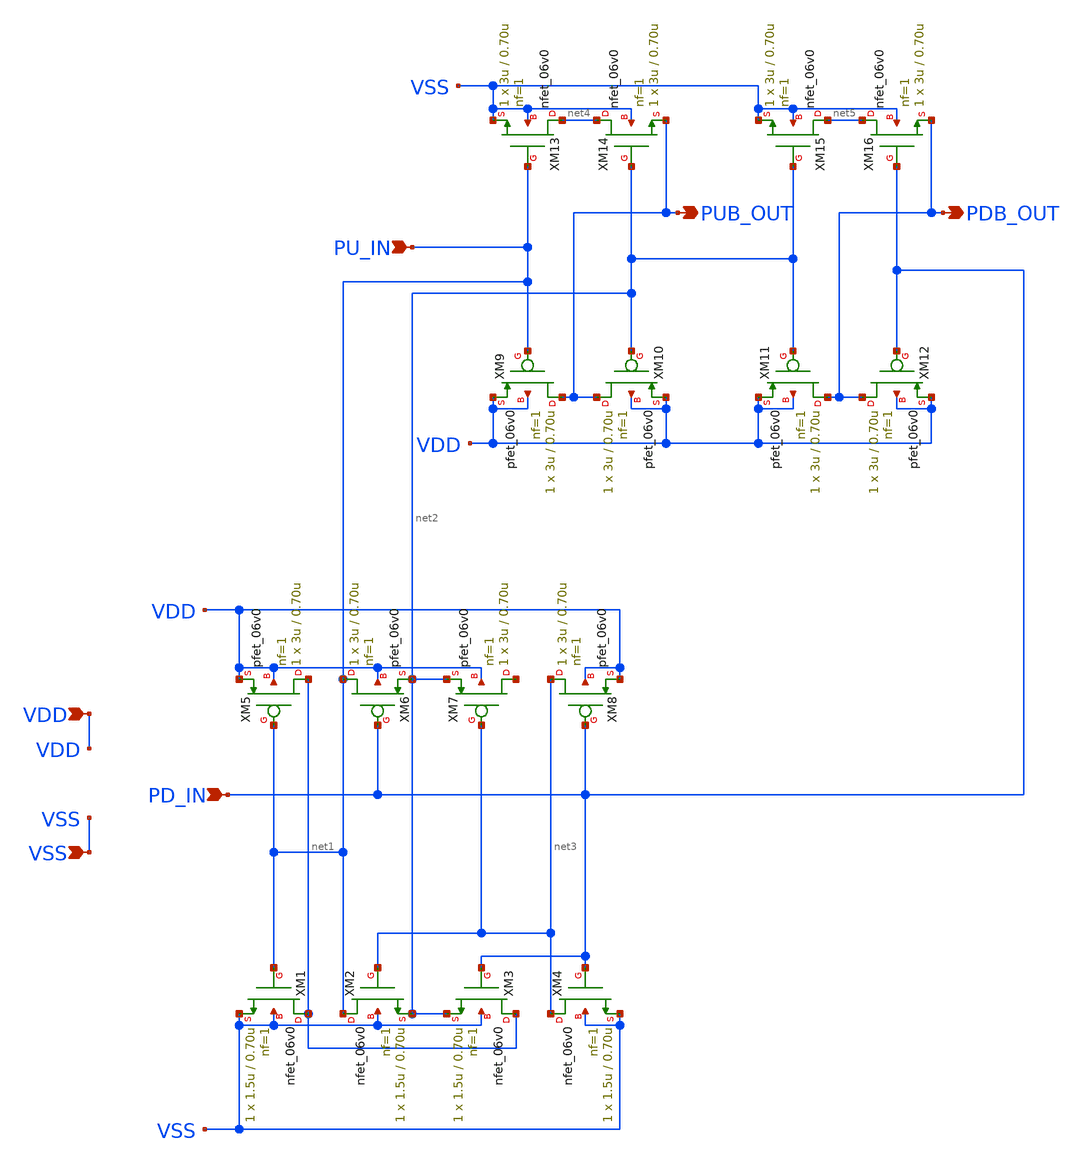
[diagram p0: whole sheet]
** sch_path: gf180mcu_fd_io__bi_24t/comp018green_in_logic_pupd.sch
**.subckt comp018green_in_logic_pupd VDD VSS PD_IN PU_IN PUB_OUT PDB_OUT
*.ipin VDD
*.ipin VSS
*.ipin PD_IN
*.ipin PU_IN
*.opin PUB_OUT
*.opin PDB_OUT
XM1 net1 PU_IN VSS VSS nfet_06v0 L=0.70u W=1.5u nf=1 ad='int((nf+1)/2) * W/nf * 0.18u' as='int((nf+2)/2) * W/nf * 0.18u'
+ pd='2*int((nf+1)/2) * (W/nf + 0.18u)' ps='2*int((nf+2)/2) * (W/nf + 0.18u)' nrd='0.18u / W' nrs='0.18u / W'
+ sa=0 sb=0 sd=0 m=1
XM2 PU_IN net3 net2 VSS nfet_06v0 L=0.70u W=1.5u nf=1 ad='int((nf+1)/2) * W/nf * 0.18u' as='int((nf+2)/2) * W/nf * 0.18u'
+ pd='2*int((nf+1)/2) * (W/nf + 0.18u)' ps='2*int((nf+2)/2) * (W/nf + 0.18u)' nrd='0.18u / W' nrs='0.18u / W'
+ sa=0 sb=0 sd=0 m=1
XM3 net1 PD_IN net2 VSS nfet_06v0 L=0.70u W=1.5u nf=1 ad='int((nf+1)/2) * W/nf * 0.18u' as='int((nf+2)/2) * W/nf * 0.18u'
+ pd='2*int((nf+1)/2) * (W/nf + 0.18u)' ps='2*int((nf+2)/2) * (W/nf + 0.18u)' nrd='0.18u / W' nrs='0.18u / W'
+ sa=0 sb=0 sd=0 m=1
XM4 net3 PD_IN VSS VSS nfet_06v0 L=0.70u W=1.5u nf=1 ad='int((nf+1)/2) * W/nf * 0.18u' as='int((nf+2)/2) * W/nf * 0.18u'
+ pd='2*int((nf+1)/2) * (W/nf + 0.18u)' ps='2*int((nf+2)/2) * (W/nf + 0.18u)' nrd='0.18u / W' nrs='0.18u / W'
+ sa=0 sb=0 sd=0 m=1
XM5 net1 PU_IN VDD VDD pfet_06v0 L=0.70u W=3u nf=1 ad='int((nf+1)/2) * W/nf * 0.18u' as='int((nf+2)/2) * W/nf * 0.18u'
+ pd='2*int((nf+1)/2) * (W/nf + 0.18u)' ps='2*int((nf+2)/2) * (W/nf + 0.18u)' nrd='0.18u / W' nrs='0.18u / W'
+ sa=0 sb=0 sd=0 m=1
XM6 PU_IN PD_IN net2 VDD pfet_06v0 L=0.70u W=3u nf=1 ad='int((nf+1)/2) * W/nf * 0.18u' as='int((nf+2)/2) * W/nf * 0.18u'
+ pd='2*int((nf+1)/2) * (W/nf + 0.18u)' ps='2*int((nf+2)/2) * (W/nf + 0.18u)' nrd='0.18u / W' nrs='0.18u / W'
+ sa=0 sb=0 sd=0 m=1
XM7 net6 net3 net2 VDD pfet_06v0 L=0.70u W=3u nf=1 ad='int((nf+1)/2) * W/nf * 0.18u' as='int((nf+2)/2) * W/nf * 0.18u'
+ pd='2*int((nf+1)/2) * (W/nf + 0.18u)' ps='2*int((nf+2)/2) * (W/nf + 0.18u)' nrd='0.18u / W' nrs='0.18u / W'
+ sa=0 sb=0 sd=0 m=1
XM8 net3 PD_IN VDD VDD pfet_06v0 L=0.70u W=3u nf=1 ad='int((nf+1)/2) * W/nf * 0.18u' as='int((nf+2)/2) * W/nf * 0.18u'
+ pd='2*int((nf+1)/2) * (W/nf + 0.18u)' ps='2*int((nf+2)/2) * (W/nf + 0.18u)' nrd='0.18u / W' nrs='0.18u / W'
+ sa=0 sb=0 sd=0 m=1
XM9 PUB_OUT PU_IN VDD VDD pfet_06v0 L=0.70u W=3u nf=1 ad='int((nf+1)/2) * W/nf * 0.18u' as='int((nf+2)/2) * W/nf * 0.18u'
+ pd='2*int((nf+1)/2) * (W/nf + 0.18u)' ps='2*int((nf+2)/2) * (W/nf + 0.18u)' nrd='0.18u / W' nrs='0.18u / W'
+ sa=0 sb=0 sd=0 m=1
XM10 PUB_OUT net2 VDD VDD pfet_06v0 L=0.70u W=3u nf=1 ad='int((nf+1)/2) * W/nf * 0.18u' as='int((nf+2)/2) * W/nf * 0.18u'
+ pd='2*int((nf+1)/2) * (W/nf + 0.18u)' ps='2*int((nf+2)/2) * (W/nf + 0.18u)' nrd='0.18u / W' nrs='0.18u / W'
+ sa=0 sb=0 sd=0 m=1
XM11 PDB_OUT net2 VDD VDD pfet_06v0 L=0.70u W=3u nf=1 ad='int((nf+1)/2) * W/nf * 0.18u' as='int((nf+2)/2) * W/nf * 0.18u'
+ pd='2*int((nf+1)/2) * (W/nf + 0.18u)' ps='2*int((nf+2)/2) * (W/nf + 0.18u)' nrd='0.18u / W' nrs='0.18u / W'
+ sa=0 sb=0 sd=0 m=1
XM12 PDB_OUT PD_IN VDD VDD pfet_06v0 L=0.70u W=3u nf=1 ad='int((nf+1)/2) * W/nf * 0.18u' as='int((nf+2)/2) * W/nf * 0.18u'
+ pd='2*int((nf+1)/2) * (W/nf + 0.18u)' ps='2*int((nf+2)/2) * (W/nf + 0.18u)' nrd='0.18u / W' nrs='0.18u / W'
+ sa=0 sb=0 sd=0 m=1
XM13 net4 PU_IN VSS VSS nfet_06v0 L=0.70u W=3u nf=1 ad='int((nf+1)/2) * W/nf * 0.18u' as='int((nf+2)/2) * W/nf * 0.18u'
+ pd='2*int((nf+1)/2) * (W/nf + 0.18u)' ps='2*int((nf+2)/2) * (W/nf + 0.18u)' nrd='0.18u / W' nrs='0.18u / W'
+ sa=0 sb=0 sd=0 m=1
XM14 net4 net2 PUB_OUT VSS nfet_06v0 L=0.70u W=3u nf=1 ad='int((nf+1)/2) * W/nf * 0.18u' as='int((nf+2)/2) * W/nf * 0.18u'
+ pd='2*int((nf+1)/2) * (W/nf + 0.18u)' ps='2*int((nf+2)/2) * (W/nf + 0.18u)' nrd='0.18u / W' nrs='0.18u / W'
+ sa=0 sb=0 sd=0 m=1
XM15 net5 net2 VSS VSS nfet_06v0 L=0.70u W=3u nf=1 ad='int((nf+1)/2) * W/nf * 0.18u' as='int((nf+2)/2) * W/nf * 0.18u'
+ pd='2*int((nf+1)/2) * (W/nf + 0.18u)' ps='2*int((nf+2)/2) * (W/nf + 0.18u)' nrd='0.18u / W' nrs='0.18u / W'
+ sa=0 sb=0 sd=0 m=1
XM16 net5 PD_IN PDB_OUT VSS nfet_06v0 L=0.70u W=3u nf=1 ad='int((nf+1)/2) * W/nf * 0.18u' as='int((nf+2)/2) * W/nf * 0.18u'
+ pd='2*int((nf+1)/2) * (W/nf + 0.18u)' ps='2*int((nf+2)/2) * (W/nf + 0.18u)' nrd='0.18u / W' nrs='0.18u / W'
+ sa=0 sb=0 sd=0 m=1
**.ends
.end
